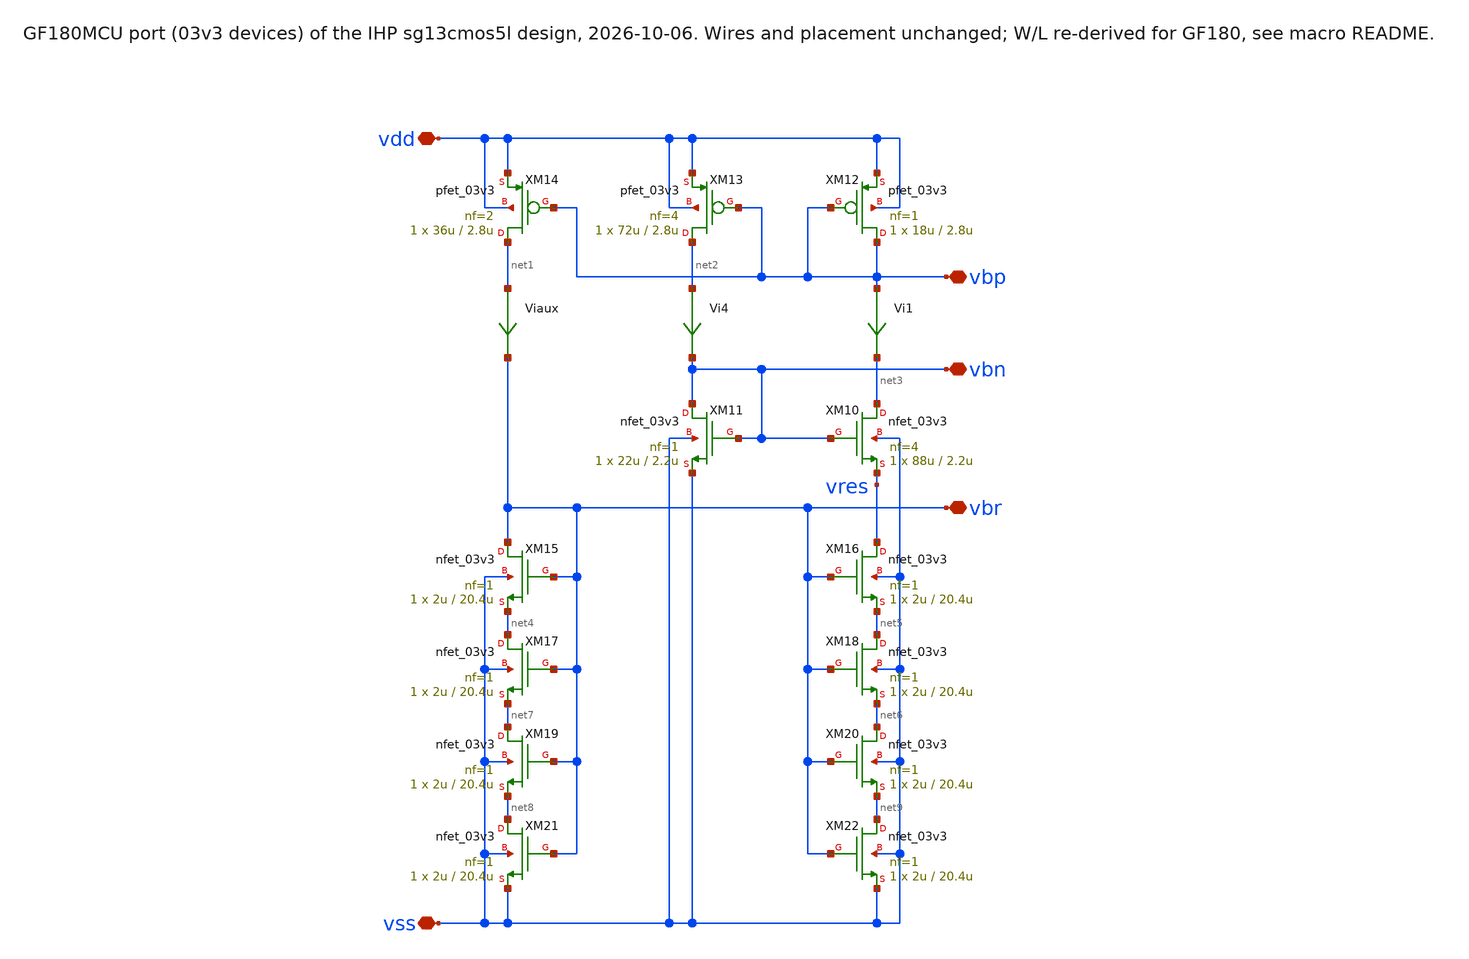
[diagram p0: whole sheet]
** sch_path: macros/OgueyAebischerBias/schematic/xschem/OgueyAebischerBias_03v3.sch
**.subckt OgueyAebischerBias_03v3 vss vdd vbp vbn vbr
*.iopin vss
*.iopin vdd
*.iopin vbp
*.iopin vbn
*.iopin vbr
XM10 net3 vbn vres vss nfet_03v3 L=2.2u W=88u nf=4 ad='int((nf+1)/2) * W/nf * 0.18u' as='int((nf+2)/2) * W/nf * 0.18u'
+ pd='2*int((nf+1)/2) * (W/nf + 0.18u)' ps='2*int((nf+2)/2) * (W/nf + 0.18u)' nrd='0.18u / W' nrs='0.18u / W'
+ sa=0 sb=0 sd=0 m=1
XM12 vbp vbp vdd vdd pfet_03v3 L=2.8u W=18u nf=1 ad='int((nf+1)/2) * W/nf * 0.18u' as='int((nf+2)/2) * W/nf * 0.18u'
+ pd='2*int((nf+1)/2) * (W/nf + 0.18u)' ps='2*int((nf+2)/2) * (W/nf + 0.18u)' nrd='0.18u / W' nrs='0.18u / W'
+ sa=0 sb=0 sd=0 m=1
XM11 vbn vbn vss vss nfet_03v3 L=2.2u W=22u nf=1 ad='int((nf+1)/2) * W/nf * 0.18u' as='int((nf+2)/2) * W/nf * 0.18u'
+ pd='2*int((nf+1)/2) * (W/nf + 0.18u)' ps='2*int((nf+2)/2) * (W/nf + 0.18u)' nrd='0.18u / W' nrs='0.18u / W'
+ sa=0 sb=0 sd=0 m=1
XM13 net2 vbp vdd vdd pfet_03v3 L=2.8u W=72u nf=4 ad='int((nf+1)/2) * W/nf * 0.18u' as='int((nf+2)/2) * W/nf * 0.18u'
+ pd='2*int((nf+1)/2) * (W/nf + 0.18u)' ps='2*int((nf+2)/2) * (W/nf + 0.18u)' nrd='0.18u / W' nrs='0.18u / W'
+ sa=0 sb=0 sd=0 m=1
XM14 net1 vbp vdd vdd pfet_03v3 L=2.8u W=36u nf=2 ad='int((nf+1)/2) * W/nf * 0.18u' as='int((nf+2)/2) * W/nf * 0.18u'
+ pd='2*int((nf+1)/2) * (W/nf + 0.18u)' ps='2*int((nf+2)/2) * (W/nf + 0.18u)' nrd='0.18u / W' nrs='0.18u / W'
+ sa=0 sb=0 sd=0 m=1
XM16 vres vbr net5 vss nfet_03v3 L=20.4u W=2u nf=1 ad='int((nf+1)/2) * W/nf * 0.18u' as='int((nf+2)/2) * W/nf * 0.18u'
+ pd='2*int((nf+1)/2) * (W/nf + 0.18u)' ps='2*int((nf+2)/2) * (W/nf + 0.18u)' nrd='0.18u / W' nrs='0.18u / W'
+ sa=0 sb=0 sd=0 m=1
XM15 vbr vbr net4 vss nfet_03v3 L=20.4u W=2u nf=1 ad='int((nf+1)/2) * W/nf * 0.18u' as='int((nf+2)/2) * W/nf * 0.18u'
+ pd='2*int((nf+1)/2) * (W/nf + 0.18u)' ps='2*int((nf+2)/2) * (W/nf + 0.18u)' nrd='0.18u / W' nrs='0.18u / W'
+ sa=0 sb=0 sd=0 m=1
Vi1 vbp net3 0
.save i(vi1)
Vi4 net2 vbn 0
.save i(vi4)
Viaux net1 vbr 0
.save i(viaux)
XM18 net5 vbr net6 vss nfet_03v3 L=20.4u W=2u nf=1 ad='int((nf+1)/2) * W/nf * 0.18u' as='int((nf+2)/2) * W/nf * 0.18u'
+ pd='2*int((nf+1)/2) * (W/nf + 0.18u)' ps='2*int((nf+2)/2) * (W/nf + 0.18u)' nrd='0.18u / W' nrs='0.18u / W'
+ sa=0 sb=0 sd=0 m=1
XM17 net4 vbr net7 vss nfet_03v3 L=20.4u W=2u nf=1 ad='int((nf+1)/2) * W/nf * 0.18u' as='int((nf+2)/2) * W/nf * 0.18u'
+ pd='2*int((nf+1)/2) * (W/nf + 0.18u)' ps='2*int((nf+2)/2) * (W/nf + 0.18u)' nrd='0.18u / W' nrs='0.18u / W'
+ sa=0 sb=0 sd=0 m=1
XM20 net6 vbr net9 vss nfet_03v3 L=20.4u W=2u nf=1 ad='int((nf+1)/2) * W/nf * 0.18u' as='int((nf+2)/2) * W/nf * 0.18u'
+ pd='2*int((nf+1)/2) * (W/nf + 0.18u)' ps='2*int((nf+2)/2) * (W/nf + 0.18u)' nrd='0.18u / W' nrs='0.18u / W'
+ sa=0 sb=0 sd=0 m=1
XM19 net7 vbr net8 vss nfet_03v3 L=20.4u W=2u nf=1 ad='int((nf+1)/2) * W/nf * 0.18u' as='int((nf+2)/2) * W/nf * 0.18u'
+ pd='2*int((nf+1)/2) * (W/nf + 0.18u)' ps='2*int((nf+2)/2) * (W/nf + 0.18u)' nrd='0.18u / W' nrs='0.18u / W'
+ sa=0 sb=0 sd=0 m=1
XM22 net9 vbr vss vss nfet_03v3 L=20.4u W=2u nf=1 ad='int((nf+1)/2) * W/nf * 0.18u' as='int((nf+2)/2) * W/nf * 0.18u'
+ pd='2*int((nf+1)/2) * (W/nf + 0.18u)' ps='2*int((nf+2)/2) * (W/nf + 0.18u)' nrd='0.18u / W' nrs='0.18u / W'
+ sa=0 sb=0 sd=0 m=1
XM21 net8 vbr vss vss nfet_03v3 L=20.4u W=2u nf=1 ad='int((nf+1)/2) * W/nf * 0.18u' as='int((nf+2)/2) * W/nf * 0.18u'
+ pd='2*int((nf+1)/2) * (W/nf + 0.18u)' ps='2*int((nf+2)/2) * (W/nf + 0.18u)' nrd='0.18u / W' nrs='0.18u / W'
+ sa=0 sb=0 sd=0 m=1
**.ends
.end
